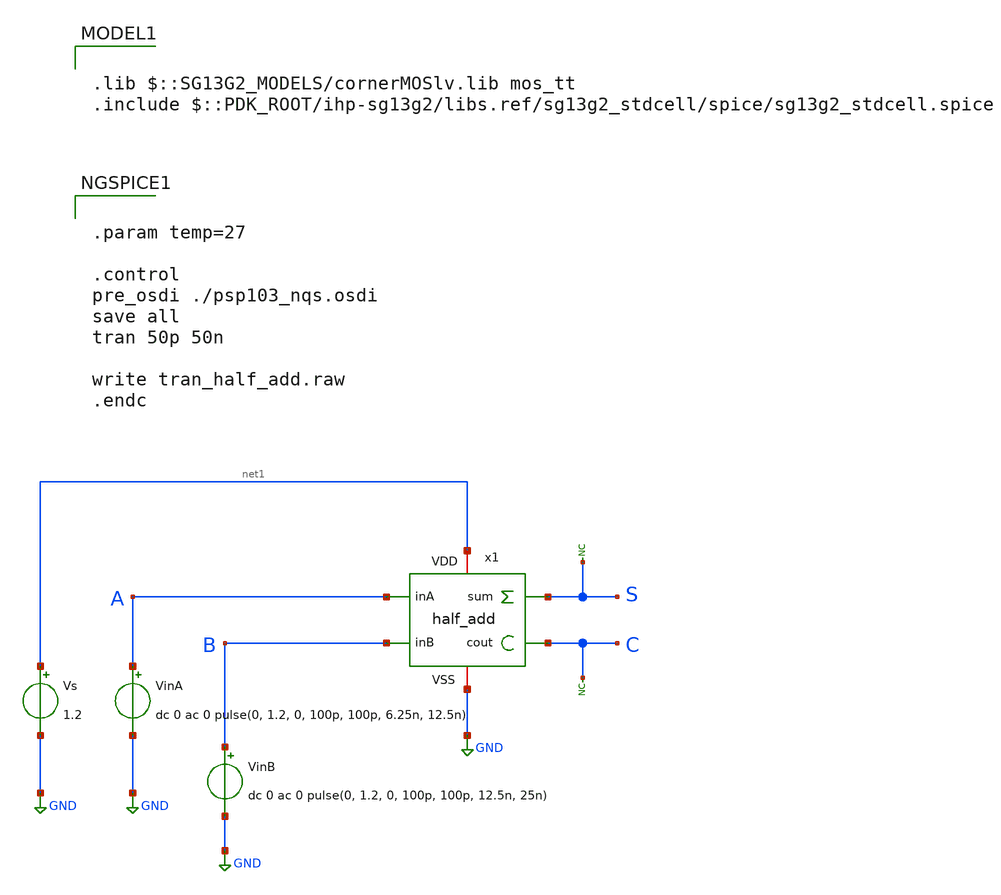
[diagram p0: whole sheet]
** sch_path: Combined Design/design_data/xschem/half_add_tb.sch

.lib $::SG13G2_MODELS/cornerMOSlv.lib mos_tt
.include $::PDK_ROOT/ihp-sg13g2/libs.ref/sg13g2_stdcell/spice/sg13g2_stdcell.spice

**.subckt half_add_tb
VinA A GND dc 0 ac 0 pulse(0, 1.2, 0, 100p, 100p, 6.25n, 12.5n)
VinB B GND dc 0 ac 0 pulse(0, 1.2, 0, 100p, 100p, 12.5n, 25n)
Vs net1 GND 1.2
* noconn S
* noconn C
x1 A S B net1 GND C half_add
**** begin user architecture code


.param temp=27

.control
pre_osdi ./psp103_nqs.osdi
save all
tran 50p 50n

write tran_half_add.raw
.endc


**** end user architecture code
**.ends
.GLOBAL GND
.end
